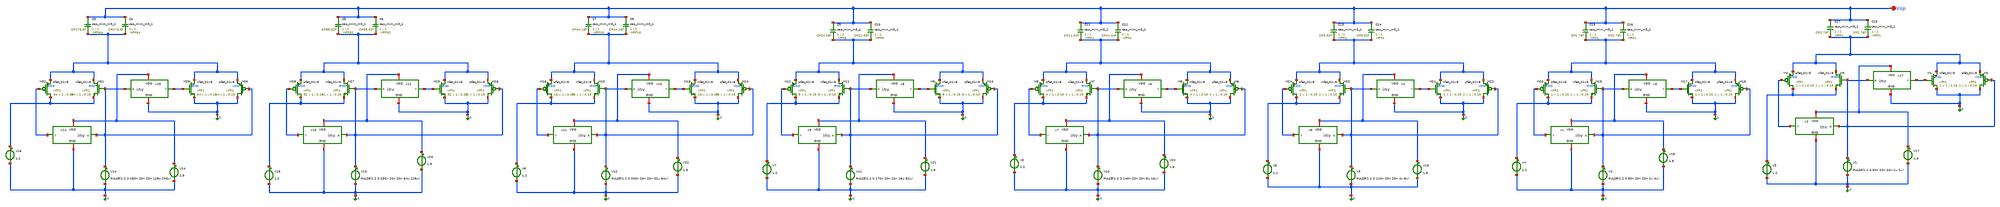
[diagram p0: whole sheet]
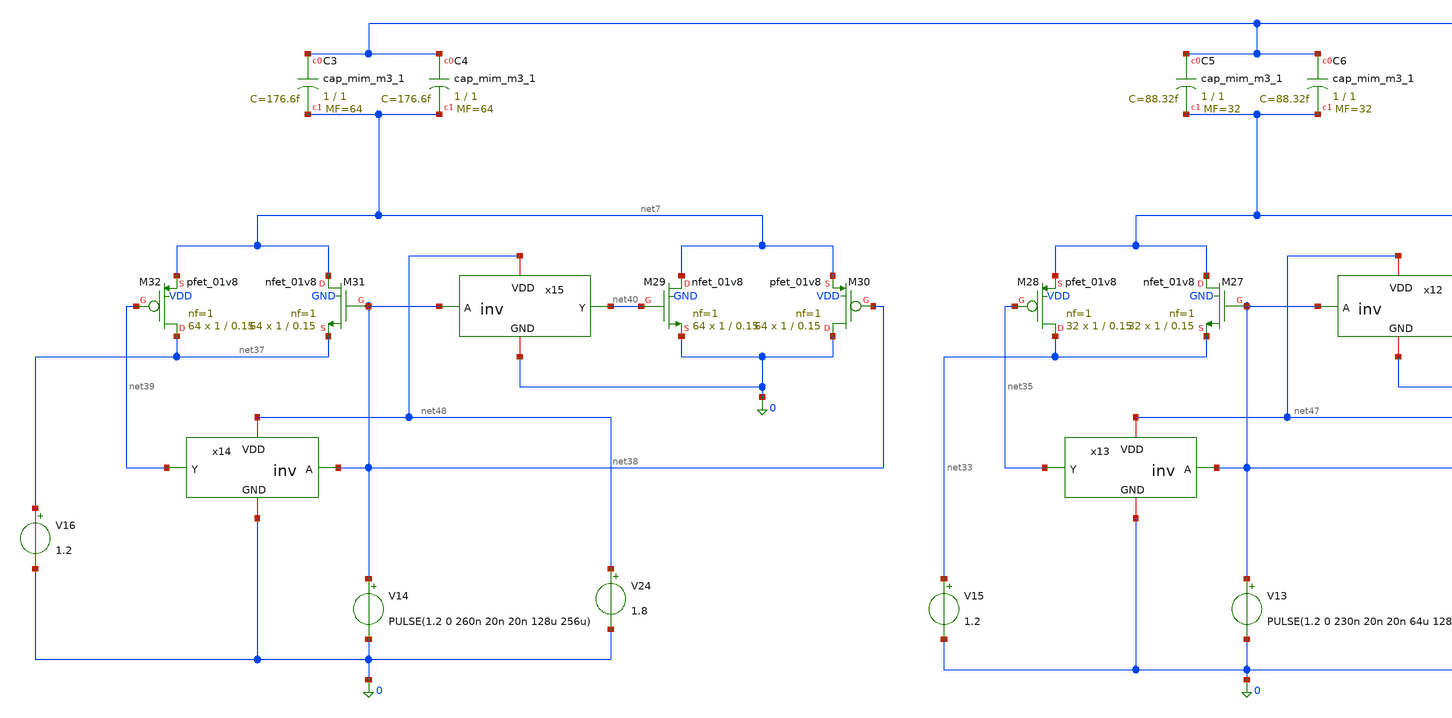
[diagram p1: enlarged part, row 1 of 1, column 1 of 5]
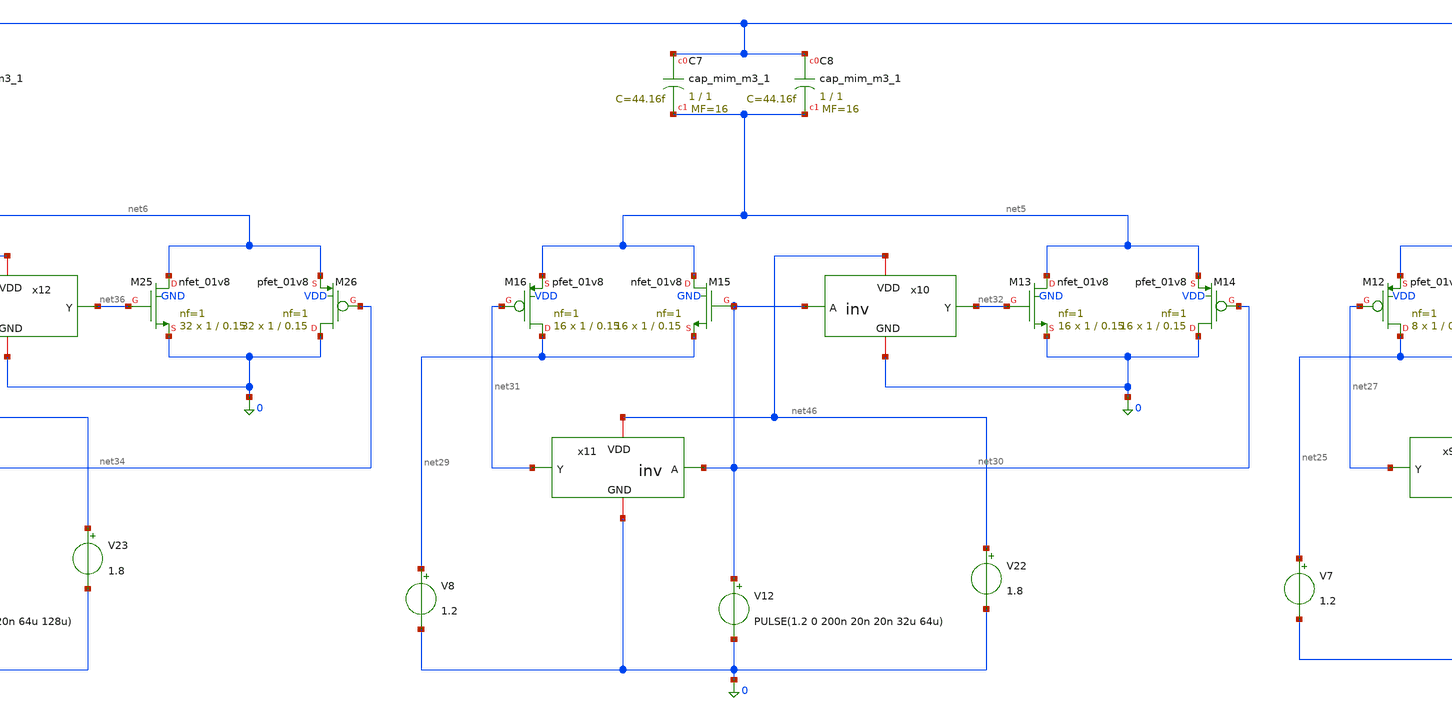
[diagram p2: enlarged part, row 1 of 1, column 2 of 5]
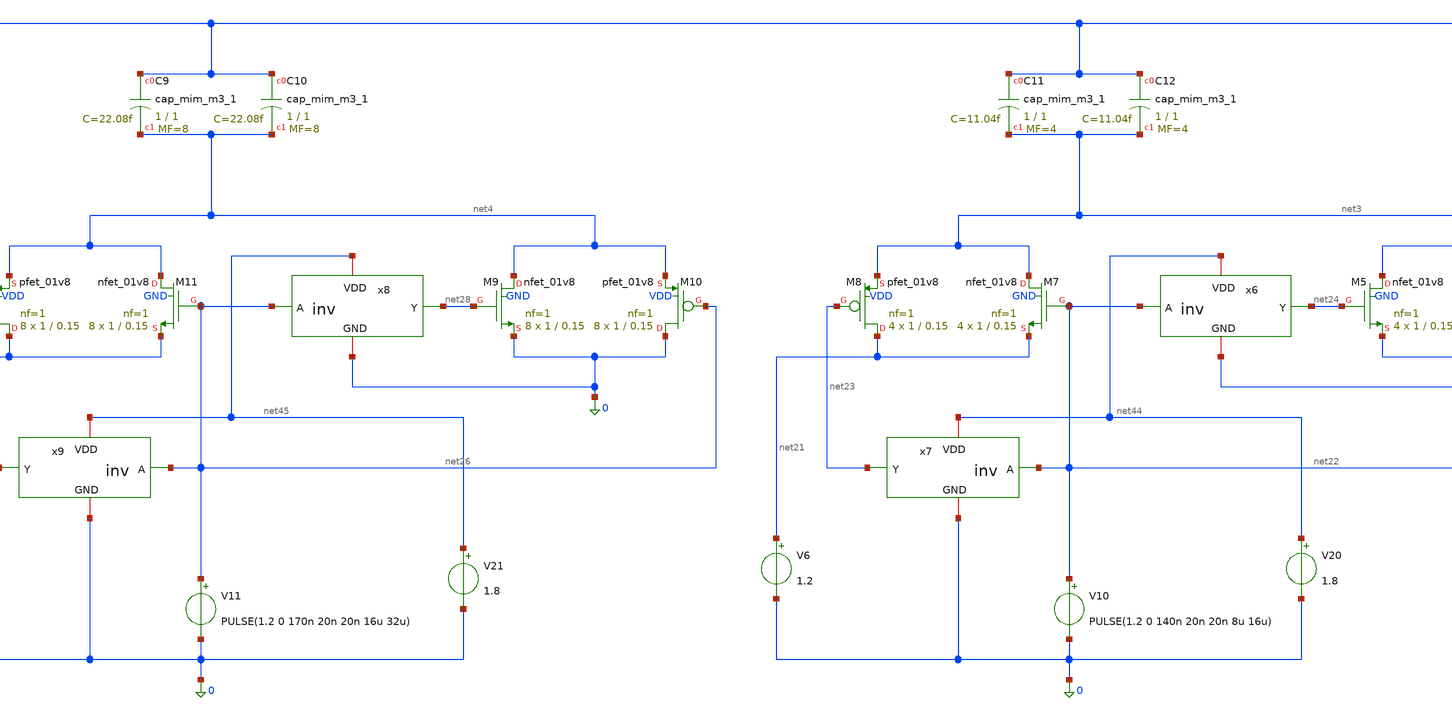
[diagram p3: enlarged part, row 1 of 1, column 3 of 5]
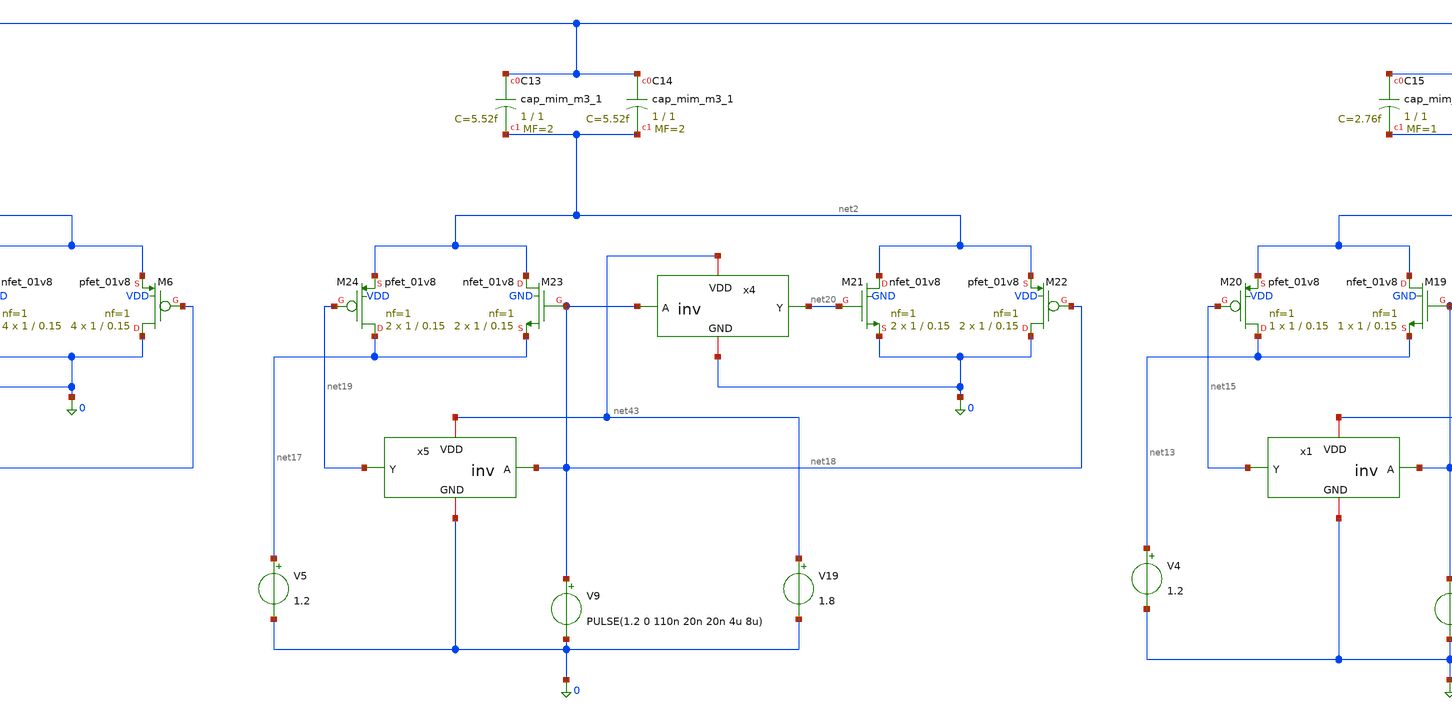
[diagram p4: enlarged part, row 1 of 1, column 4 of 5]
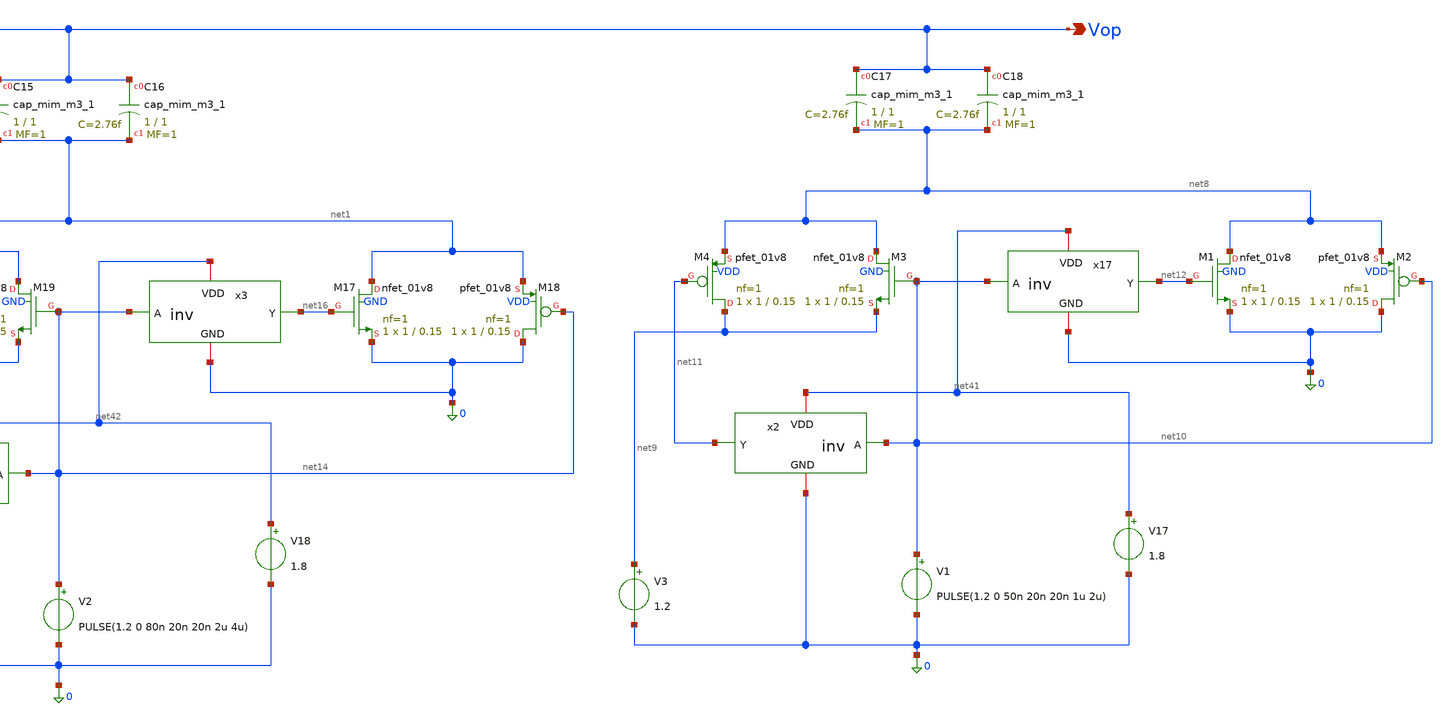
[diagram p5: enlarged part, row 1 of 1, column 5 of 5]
** sch_path: sar-adc/cdac_2.sch
**.subckt cdac_2 Vop
*.opin Vop
XC3 Vop net7 sky130_fd_pr__cap_mim_m3_1 W=1 L=1 MF=64 m=64
XC4 Vop net7 sky130_fd_pr__cap_mim_m3_1 W=1 L=1 MF=64 m=64
XC5 Vop net6 sky130_fd_pr__cap_mim_m3_1 W=1 L=1 MF=32 m=32
XC6 Vop net6 sky130_fd_pr__cap_mim_m3_1 W=1 L=1 MF=32 m=32
XC7 Vop net5 sky130_fd_pr__cap_mim_m3_1 W=1 L=1 MF=16 m=16
XC8 Vop net5 sky130_fd_pr__cap_mim_m3_1 W=1 L=1 MF=16 m=16
XC9 Vop net4 sky130_fd_pr__cap_mim_m3_1 W=1 L=1 MF=8 m=8
XC10 Vop net4 sky130_fd_pr__cap_mim_m3_1 W=1 L=1 MF=8 m=8
XC11 Vop net3 sky130_fd_pr__cap_mim_m3_1 W=1 L=1 MF=4 m=4
XC12 Vop net3 sky130_fd_pr__cap_mim_m3_1 W=1 L=1 MF=4 m=4
XC13 Vop net2 sky130_fd_pr__cap_mim_m3_1 W=1 L=1 MF=2 m=2
XC14 Vop net2 sky130_fd_pr__cap_mim_m3_1 W=1 L=1 MF=2 m=2
XC15 Vop net1 sky130_fd_pr__cap_mim_m3_1 W=1 L=1 MF=1 m=1
XC16 Vop net1 sky130_fd_pr__cap_mim_m3_1 W=1 L=1 MF=1 m=1
XC17 Vop net8 sky130_fd_pr__cap_mim_m3_1 W=1 L=1 MF=1 m=1
XC18 Vop net8 sky130_fd_pr__cap_mim_m3_1 W=1 L=1 MF=1 m=1
XM1 net8 net12 0 GND sky130_fd_pr__nfet_01v8 L=0.15 W=1 nf=1 ad='int((1 + 1)/2) * 1 / 1 * 0.29' as='int((1 + 2)/2) * 1 / 1 * 0.29'
+ pd='2*int((1 + 1)/2) * (1 / 1 + 0.29)' ps='2*int((1 + 2)/2) * (1 / 1 + 0.29)' nrd='0.29 / 1 ' nrs='0.29 / 1 '
+ sa=0 sb=0 sd=0 mult=1 m=1
XM2 0 net10 net8 VDD sky130_fd_pr__pfet_01v8 L=0.15 W=1 nf=1 ad='int((1 + 1)/2) * 1 / 1 * 0.29' as='int((1 + 2)/2) * 1 / 1 * 0.29'
+ pd='2*int((1 + 1)/2) * (1 / 1 + 0.29)' ps='2*int((1 + 2)/2) * (1 / 1 + 0.29)' nrd='0.29 / 1 ' nrs='0.29 / 1 '
+ sa=0 sb=0 sd=0 mult=1 m=1
XM3 net8 net10 net9 GND sky130_fd_pr__nfet_01v8 L=0.15 W=1 nf=1 ad='int((1 + 1)/2) * 1 / 1 * 0.29' as='int((1 + 2)/2) * 1 / 1 * 0.29'
+ pd='2*int((1 + 1)/2) * (1 / 1 + 0.29)' ps='2*int((1 + 2)/2) * (1 / 1 + 0.29)' nrd='0.29 / 1 ' nrs='0.29 / 1 '
+ sa=0 sb=0 sd=0 mult=1 m=1
XM4 net9 net11 net8 VDD sky130_fd_pr__pfet_01v8 L=0.15 W=1 nf=1 ad='int((1 + 1)/2) * 1 / 1 * 0.29' as='int((1 + 2)/2) * 1 / 1 * 0.29'
+ pd='2*int((1 + 1)/2) * (1 / 1 + 0.29)' ps='2*int((1 + 2)/2) * (1 / 1 + 0.29)' nrd='0.29 / 1 ' nrs='0.29 / 1 '
+ sa=0 sb=0 sd=0 mult=1 m=1
V1 net10 0 PULSE(1.2 0 50n 20n 20n 1u 2u)
XM17 net1 net16 0 GND sky130_fd_pr__nfet_01v8 L=0.15 W=1 nf=1 ad='int((1 + 1)/2) * 1 / 1 * 0.29' as='int((1 + 2)/2) * 1 / 1 * 0.29'
+ pd='2*int((1 + 1)/2) * (1 / 1 + 0.29)' ps='2*int((1 + 2)/2) * (1 / 1 + 0.29)' nrd='0.29 / 1 ' nrs='0.29 / 1 '
+ sa=0 sb=0 sd=0 mult=1 m=1
XM18 0 net14 net1 VDD sky130_fd_pr__pfet_01v8 L=0.15 W=1 nf=1 ad='int((1 + 1)/2) * 1 / 1 * 0.29' as='int((1 + 2)/2) * 1 / 1 * 0.29'
+ pd='2*int((1 + 1)/2) * (1 / 1 + 0.29)' ps='2*int((1 + 2)/2) * (1 / 1 + 0.29)' nrd='0.29 / 1 ' nrs='0.29 / 1 '
+ sa=0 sb=0 sd=0 mult=1 m=1
XM19 net1 net14 net13 GND sky130_fd_pr__nfet_01v8 L=0.15 W=1 nf=1 ad='int((1 + 1)/2) * 1 / 1 * 0.29'
+ as='int((1 + 2)/2) * 1 / 1 * 0.29' pd='2*int((1 + 1)/2) * (1 / 1 + 0.29)' ps='2*int((1 + 2)/2) * (1 / 1 + 0.29)'
+ nrd='0.29 / 1 ' nrs='0.29 / 1 ' sa=0 sb=0 sd=0 mult=1 m=1
XM20 net13 net15 net1 VDD sky130_fd_pr__pfet_01v8 L=0.15 W=1 nf=1 ad='int((1 + 1)/2) * 1 / 1 * 0.29'
+ as='int((1 + 2)/2) * 1 / 1 * 0.29' pd='2*int((1 + 1)/2) * (1 / 1 + 0.29)' ps='2*int((1 + 2)/2) * (1 / 1 + 0.29)'
+ nrd='0.29 / 1 ' nrs='0.29 / 1 ' sa=0 sb=0 sd=0 mult=1 m=1
XM21 net2 net20 0 GND sky130_fd_pr__nfet_01v8 L=0.15 W=1 nf=1 ad='int((1 + 1)/2) * 1 / 1 * 0.29' as='int((1 + 2)/2) * 1 / 1 * 0.29'
+ pd='2*int((1 + 1)/2) * (1 / 1 + 0.29)' ps='2*int((1 + 2)/2) * (1 / 1 + 0.29)' nrd='0.29 / 1 ' nrs='0.29 / 1 '
+ sa=0 sb=0 sd=0 mult=2 m=2
XM22 0 net18 net2 VDD sky130_fd_pr__pfet_01v8 L=0.15 W=1 nf=1 ad='int((1 + 1)/2) * 1 / 1 * 0.29' as='int((1 + 2)/2) * 1 / 1 * 0.29'
+ pd='2*int((1 + 1)/2) * (1 / 1 + 0.29)' ps='2*int((1 + 2)/2) * (1 / 1 + 0.29)' nrd='0.29 / 1 ' nrs='0.29 / 1 '
+ sa=0 sb=0 sd=0 mult=2 m=2
XM23 net2 net18 net17 GND sky130_fd_pr__nfet_01v8 L=0.15 W=1 nf=1 ad='int((1 + 1)/2) * 1 / 1 * 0.29'
+ as='int((1 + 2)/2) * 1 / 1 * 0.29' pd='2*int((1 + 1)/2) * (1 / 1 + 0.29)' ps='2*int((1 + 2)/2) * (1 / 1 + 0.29)'
+ nrd='0.29 / 1 ' nrs='0.29 / 1 ' sa=0 sb=0 sd=0 mult=2 m=2
XM24 net17 net19 net2 VDD sky130_fd_pr__pfet_01v8 L=0.15 W=1 nf=1 ad='int((1 + 1)/2) * 1 / 1 * 0.29'
+ as='int((1 + 2)/2) * 1 / 1 * 0.29' pd='2*int((1 + 1)/2) * (1 / 1 + 0.29)' ps='2*int((1 + 2)/2) * (1 / 1 + 0.29)'
+ nrd='0.29 / 1 ' nrs='0.29 / 1 ' sa=0 sb=0 sd=0 mult=2 m=2
XM5 net3 net24 0 GND sky130_fd_pr__nfet_01v8 L=0.15 W=1 nf=1 ad='int((1 + 1)/2) * 1 / 1 * 0.29' as='int((1 + 2)/2) * 1 / 1 * 0.29'
+ pd='2*int((1 + 1)/2) * (1 / 1 + 0.29)' ps='2*int((1 + 2)/2) * (1 / 1 + 0.29)' nrd='0.29 / 1 ' nrs='0.29 / 1 '
+ sa=0 sb=0 sd=0 mult=4 m=4
XM6 0 net22 net3 VDD sky130_fd_pr__pfet_01v8 L=0.15 W=1 nf=1 ad='int((1 + 1)/2) * 1 / 1 * 0.29' as='int((1 + 2)/2) * 1 / 1 * 0.29'
+ pd='2*int((1 + 1)/2) * (1 / 1 + 0.29)' ps='2*int((1 + 2)/2) * (1 / 1 + 0.29)' nrd='0.29 / 1 ' nrs='0.29 / 1 '
+ sa=0 sb=0 sd=0 mult=4 m=4
XM7 net3 net22 net21 GND sky130_fd_pr__nfet_01v8 L=0.15 W=1 nf=1 ad='int((1 + 1)/2) * 1 / 1 * 0.29' as='int((1 + 2)/2) * 1 / 1 * 0.29'
+ pd='2*int((1 + 1)/2) * (1 / 1 + 0.29)' ps='2*int((1 + 2)/2) * (1 / 1 + 0.29)' nrd='0.29 / 1 ' nrs='0.29 / 1 '
+ sa=0 sb=0 sd=0 mult=4 m=4
XM8 net21 net23 net3 VDD sky130_fd_pr__pfet_01v8 L=0.15 W=1 nf=1 ad='int((1 + 1)/2) * 1 / 1 * 0.29' as='int((1 + 2)/2) * 1 / 1 * 0.29'
+ pd='2*int((1 + 1)/2) * (1 / 1 + 0.29)' ps='2*int((1 + 2)/2) * (1 / 1 + 0.29)' nrd='0.29 / 1 ' nrs='0.29 / 1 '
+ sa=0 sb=0 sd=0 mult=4 m=4
XM9 net4 net28 0 GND sky130_fd_pr__nfet_01v8 L=0.15 W=1 nf=1 ad='int((1 + 1)/2) * 1 / 1 * 0.29' as='int((1 + 2)/2) * 1 / 1 * 0.29'
+ pd='2*int((1 + 1)/2) * (1 / 1 + 0.29)' ps='2*int((1 + 2)/2) * (1 / 1 + 0.29)' nrd='0.29 / 1 ' nrs='0.29 / 1 '
+ sa=0 sb=0 sd=0 mult=8 m=8
XM10 0 net26 net4 VDD sky130_fd_pr__pfet_01v8 L=0.15 W=1 nf=1 ad='int((1 + 1)/2) * 1 / 1 * 0.29' as='int((1 + 2)/2) * 1 / 1 * 0.29'
+ pd='2*int((1 + 1)/2) * (1 / 1 + 0.29)' ps='2*int((1 + 2)/2) * (1 / 1 + 0.29)' nrd='0.29 / 1 ' nrs='0.29 / 1 '
+ sa=0 sb=0 sd=0 mult=8 m=8
XM11 net4 net26 net25 GND sky130_fd_pr__nfet_01v8 L=0.15 W=1 nf=1 ad='int((1 + 1)/2) * 1 / 1 * 0.29'
+ as='int((1 + 2)/2) * 1 / 1 * 0.29' pd='2*int((1 + 1)/2) * (1 / 1 + 0.29)' ps='2*int((1 + 2)/2) * (1 / 1 + 0.29)'
+ nrd='0.29 / 1 ' nrs='0.29 / 1 ' sa=0 sb=0 sd=0 mult=8 m=8
XM12 net25 net27 net4 VDD sky130_fd_pr__pfet_01v8 L=0.15 W=1 nf=1 ad='int((1 + 1)/2) * 1 / 1 * 0.29'
+ as='int((1 + 2)/2) * 1 / 1 * 0.29' pd='2*int((1 + 1)/2) * (1 / 1 + 0.29)' ps='2*int((1 + 2)/2) * (1 / 1 + 0.29)'
+ nrd='0.29 / 1 ' nrs='0.29 / 1 ' sa=0 sb=0 sd=0 mult=8 m=8
XM13 net5 net32 0 GND sky130_fd_pr__nfet_01v8 L=0.15 W=1 nf=1 ad='int((1 + 1)/2) * 1 / 1 * 0.29' as='int((1 + 2)/2) * 1 / 1 * 0.29'
+ pd='2*int((1 + 1)/2) * (1 / 1 + 0.29)' ps='2*int((1 + 2)/2) * (1 / 1 + 0.29)' nrd='0.29 / 1 ' nrs='0.29 / 1 '
+ sa=0 sb=0 sd=0 mult=16 m=16
XM14 0 net30 net5 VDD sky130_fd_pr__pfet_01v8 L=0.15 W=1 nf=1 ad='int((1 + 1)/2) * 1 / 1 * 0.29' as='int((1 + 2)/2) * 1 / 1 * 0.29'
+ pd='2*int((1 + 1)/2) * (1 / 1 + 0.29)' ps='2*int((1 + 2)/2) * (1 / 1 + 0.29)' nrd='0.29 / 1 ' nrs='0.29 / 1 '
+ sa=0 sb=0 sd=0 mult=16 m=16
XM15 net5 net30 net29 GND sky130_fd_pr__nfet_01v8 L=0.15 W=1 nf=1 ad='int((1 + 1)/2) * 1 / 1 * 0.29'
+ as='int((1 + 2)/2) * 1 / 1 * 0.29' pd='2*int((1 + 1)/2) * (1 / 1 + 0.29)' ps='2*int((1 + 2)/2) * (1 / 1 + 0.29)'
+ nrd='0.29 / 1 ' nrs='0.29 / 1 ' sa=0 sb=0 sd=0 mult=16 m=16
XM16 net29 net31 net5 VDD sky130_fd_pr__pfet_01v8 L=0.15 W=1 nf=1 ad='int((1 + 1)/2) * 1 / 1 * 0.29'
+ as='int((1 + 2)/2) * 1 / 1 * 0.29' pd='2*int((1 + 1)/2) * (1 / 1 + 0.29)' ps='2*int((1 + 2)/2) * (1 / 1 + 0.29)'
+ nrd='0.29 / 1 ' nrs='0.29 / 1 ' sa=0 sb=0 sd=0 mult=16 m=16
XM25 net6 net36 0 GND sky130_fd_pr__nfet_01v8 L=0.15 W=1 nf=1 ad='int((1 + 1)/2) * 1 / 1 * 0.29' as='int((1 + 2)/2) * 1 / 1 * 0.29'
+ pd='2*int((1 + 1)/2) * (1 / 1 + 0.29)' ps='2*int((1 + 2)/2) * (1 / 1 + 0.29)' nrd='0.29 / 1 ' nrs='0.29 / 1 '
+ sa=0 sb=0 sd=0 mult=32 m=32
XM26 0 net34 net6 VDD sky130_fd_pr__pfet_01v8 L=0.15 W=1 nf=1 ad='int((1 + 1)/2) * 1 / 1 * 0.29' as='int((1 + 2)/2) * 1 / 1 * 0.29'
+ pd='2*int((1 + 1)/2) * (1 / 1 + 0.29)' ps='2*int((1 + 2)/2) * (1 / 1 + 0.29)' nrd='0.29 / 1 ' nrs='0.29 / 1 '
+ sa=0 sb=0 sd=0 mult=32 m=32
XM27 net6 net34 net33 GND sky130_fd_pr__nfet_01v8 L=0.15 W=1 nf=1 ad='int((1 + 1)/2) * 1 / 1 * 0.29'
+ as='int((1 + 2)/2) * 1 / 1 * 0.29' pd='2*int((1 + 1)/2) * (1 / 1 + 0.29)' ps='2*int((1 + 2)/2) * (1 / 1 + 0.29)'
+ nrd='0.29 / 1 ' nrs='0.29 / 1 ' sa=0 sb=0 sd=0 mult=32 m=32
XM28 net33 net35 net6 VDD sky130_fd_pr__pfet_01v8 L=0.15 W=1 nf=1 ad='int((1 + 1)/2) * 1 / 1 * 0.29'
+ as='int((1 + 2)/2) * 1 / 1 * 0.29' pd='2*int((1 + 1)/2) * (1 / 1 + 0.29)' ps='2*int((1 + 2)/2) * (1 / 1 + 0.29)'
+ nrd='0.29 / 1 ' nrs='0.29 / 1 ' sa=0 sb=0 sd=0 mult=32 m=32
XM29 net7 net40 0 GND sky130_fd_pr__nfet_01v8 L=0.15 W=1 nf=1 ad='int((1 + 1)/2) * 1 / 1 * 0.29' as='int((1 + 2)/2) * 1 / 1 * 0.29'
+ pd='2*int((1 + 1)/2) * (1 / 1 + 0.29)' ps='2*int((1 + 2)/2) * (1 / 1 + 0.29)' nrd='0.29 / 1 ' nrs='0.29 / 1 '
+ sa=0 sb=0 sd=0 mult=64 m=64
XM30 0 net38 net7 VDD sky130_fd_pr__pfet_01v8 L=0.15 W=1 nf=1 ad='int((1 + 1)/2) * 1 / 1 * 0.29' as='int((1 + 2)/2) * 1 / 1 * 0.29'
+ pd='2*int((1 + 1)/2) * (1 / 1 + 0.29)' ps='2*int((1 + 2)/2) * (1 / 1 + 0.29)' nrd='0.29 / 1 ' nrs='0.29 / 1 '
+ sa=0 sb=0 sd=0 mult=64 m=64
XM31 net7 net38 net37 GND sky130_fd_pr__nfet_01v8 L=0.15 W=1 nf=1 ad='int((1 + 1)/2) * 1 / 1 * 0.29'
+ as='int((1 + 2)/2) * 1 / 1 * 0.29' pd='2*int((1 + 1)/2) * (1 / 1 + 0.29)' ps='2*int((1 + 2)/2) * (1 / 1 + 0.29)'
+ nrd='0.29 / 1 ' nrs='0.29 / 1 ' sa=0 sb=0 sd=0 mult=64 m=64
XM32 net37 net39 net7 VDD sky130_fd_pr__pfet_01v8 L=0.15 W=1 nf=1 ad='int((1 + 1)/2) * 1 / 1 * 0.29'
+ as='int((1 + 2)/2) * 1 / 1 * 0.29' pd='2*int((1 + 1)/2) * (1 / 1 + 0.29)' ps='2*int((1 + 2)/2) * (1 / 1 + 0.29)'
+ nrd='0.29 / 1 ' nrs='0.29 / 1 ' sa=0 sb=0 sd=0 mult=64 m=64
V2 net14 0 PULSE(1.2 0 80n 20n 20n 2u 4u)
V9 net18 0 PULSE(1.2 0 110n 20n 20n 4u 8u)
V10 net22 0 PULSE(1.2 0 140n 20n 20n 8u 16u)
V11 net26 0 PULSE(1.2 0 170n 20n 20n 16u 32u)
V12 net30 0 PULSE(1.2 0 200n 20n 20n 32u 64u)
V13 net34 0 PULSE(1.2 0 230n 20n 20n 64u 128u)
V14 net38 0 PULSE(1.2 0 260n 20n 20n 128u 256u)
V3 net9 0 1.2
V4 net13 0 1.2
V5 net17 0 1.2
V6 net21 0 1.2
V7 net25 0 1.2
V8 net29 0 1.2
V15 net33 0 1.2
V16 net37 0 1.2
V17 net41 0 1.8
V18 net42 0 1.8
V19 net43 0 1.8
V20 net44 0 1.8
V21 net45 0 1.8
V22 net46 0 1.8
V23 net47 0 1.8
V24 net48 0 1.8
x17 net41 net10 net12 0 inv
x2 net41 net10 net11 0 inv
x1 net42 net14 net15 0 inv
x3 net42 net14 net16 0 inv
x4 net43 net18 net20 0 inv
x5 net43 net18 net19 0 inv
x6 net44 net22 net24 0 inv
x7 net44 net22 net23 0 inv
x8 net45 net26 net28 0 inv
x9 net45 net26 net27 0 inv
x10 net46 net30 net32 0 inv
x11 net46 net30 net31 0 inv
x12 net47 net34 net36 0 inv
x13 net47 net34 net35 0 inv
x14 net48 net38 net39 0 inv
x15 net48 net38 net40 0 inv
**** begin user architecture code




.control

 tran 10n 270u
run
*plot v(net8) v(net1)+2 v(net2)+4 v(net3)+6 v(net4)+8 v(net5)+10 v(net6)+12 v(net7)+14 Vop+16
 .endc





.control

 tran 10n 270u
run
*plot v(net8) v(net1)+2 v(net2)+4 v(net3)+6 v(net4)+8 v(net5)+10 v(net6)+12 v(net7)+14 Vop+16
 .endc

**** end user architecture code
**.ends

* expanding   symbol:  inv.sym # of pins=4
** sym_path: sar-adc/inv.sym
** sch_path: sar-adc/inv.sch
.subckt inv VDD A Y GND
*.iopin GND
*.iopin VDD
*.ipin A
*.opin Y
XM1 Y A GND GND sky130_fd_pr__nfet_01v8 L=0.65 W=1 nf=1 ad='int((1 + 1)/2) * 1 / 1 * 0.29' as='int((1 + 2)/2) * 1 / 1 * 0.29'
+ pd='2*int((1 + 1)/2) * (1 / 1 + 0.29)' ps='2*int((1 + 2)/2) * (1 / 1 + 0.29)' nrd='0.29 / 1 ' nrs='0.29 / 1 '
+ sa=0 sb=0 sd=0 mult=1 m=1
XM2 Y A VDD VDD sky130_fd_pr__pfet_01v8 L=0.15 W=1 nf=1 ad='int((1 + 1)/2) * 1 / 1 * 0.29' as='int((1 + 2)/2) * 1 / 1 * 0.29'
+ pd='2*int((1 + 1)/2) * (1 / 1 + 0.29)' ps='2*int((1 + 2)/2) * (1 / 1 + 0.29)' nrd='0.29 / 1 ' nrs='0.29 / 1 '
+ sa=0 sb=0 sd=0 mult=1 m=1
.ends

.end
